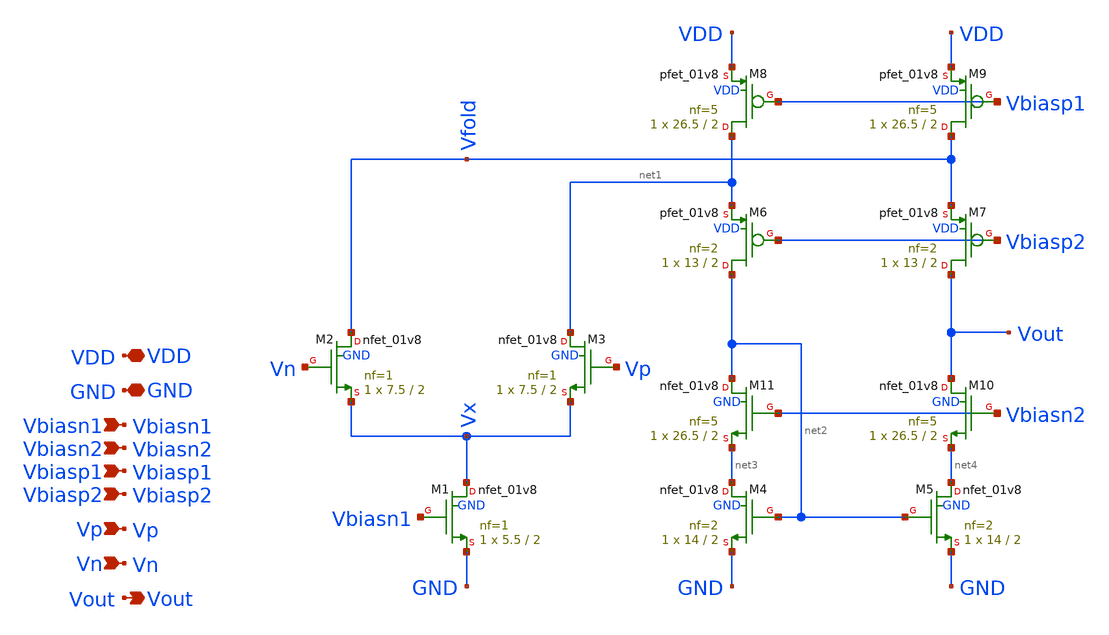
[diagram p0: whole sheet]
** sch_path: sch/cascode/ota_n.sch
**.subckt ota_n Vbiasn2 Vout VDD GND Vp Vn Vbiasp1 Vbiasp2 Vbiasn1
*.ipin Vbiasn2
*.opin Vout
*.iopin VDD
*.iopin GND
*.ipin Vp
*.ipin Vn
*.ipin Vbiasp1
*.ipin Vbiasp2
*.ipin Vbiasn1
XM3 net1 Vp Vx GND sky130_fd_pr__nfet_01v8 L=2 W=7.5 nf=1 ad='int((1 + 1)/2) * 7.5 / 1 * 0.29' as='int((1 + 2)/2) * 7.5 / 1 * 0.29'
+ pd='2*int((1 + 1)/2) * (7.5 / 1 + 0.29)' ps='2*int((1 + 2)/2) * (7.5 / 1 + 0.29)' nrd='0.29 / 7.5 ' nrs='0.29 / 7.5 '
+ sa=0 sb=0 sd=0 mult=1 m=1
XM2 Vfold Vn Vx GND sky130_fd_pr__nfet_01v8 L=2 W=7.5 nf=1 ad='int((1 + 1)/2) * 7.5 / 1 * 0.29' as='int((1 + 2)/2) * 7.5 / 1 * 0.29'
+ pd='2*int((1 + 1)/2) * (7.5 / 1 + 0.29)' ps='2*int((1 + 2)/2) * (7.5 / 1 + 0.29)' nrd='0.29 / 7.5 ' nrs='0.29 / 7.5 '
+ sa=0 sb=0 sd=0 mult=1 m=1
XM4 net3 net2 GND GND sky130_fd_pr__nfet_01v8 L=2 W=14 nf=2 ad='int((2 + 1)/2) * 14 / 2 * 0.29' as='int((2 + 2)/2) * 14 / 2 * 0.29'
+ pd='2*int((2 + 1)/2) * (14 / 2 + 0.29)' ps='2*int((2 + 2)/2) * (14 / 2 + 0.29)' nrd='0.29 / 14 ' nrs='0.29 / 14 '
+ sa=0 sb=0 sd=0 mult=1 m=1
XM5 net4 net2 GND GND sky130_fd_pr__nfet_01v8 L=2 W=14 nf=2 ad='int((2 + 1)/2) * 14 / 2 * 0.29' as='int((2 + 2)/2) * 14 / 2 * 0.29'
+ pd='2*int((2 + 1)/2) * (14 / 2 + 0.29)' ps='2*int((2 + 2)/2) * (14 / 2 + 0.29)' nrd='0.29 / 14 ' nrs='0.29 / 14 '
+ sa=0 sb=0 sd=0 mult=1 m=1
XM8 net1 Vbiasp1 VDD VDD sky130_fd_pr__pfet_01v8 L=2 W=26.5 nf=5 ad='int((5 + 1)/2) * 26.5 / 5 * 0.29'
+ as='int((5 + 2)/2) * 26.5 / 5 * 0.29' pd='2*int((5 + 1)/2) * (26.5 / 5 + 0.29)' ps='2*int((5 + 2)/2) * (26.5 / 5 + 0.29)'
+ nrd='0.29 / 26.5 ' nrs='0.29 / 26.5 ' sa=0 sb=0 sd=0 mult=1 m=1
XM9 Vfold Vbiasp1 VDD VDD sky130_fd_pr__pfet_01v8 L=2 W=26.5 nf=5 ad='int((5 + 1)/2) * 26.5 / 5 * 0.29'
+ as='int((5 + 2)/2) * 26.5 / 5 * 0.29' pd='2*int((5 + 1)/2) * (26.5 / 5 + 0.29)' ps='2*int((5 + 2)/2) * (26.5 / 5 + 0.29)'
+ nrd='0.29 / 26.5 ' nrs='0.29 / 26.5 ' sa=0 sb=0 sd=0 mult=1 m=1
XM1 Vx Vbiasn1 GND GND sky130_fd_pr__nfet_01v8 L=2 W=5.5 nf=1 ad='int((1 + 1)/2) * 5.5 / 1 * 0.29' as='int((1 + 2)/2) * 5.5 / 1 * 0.29'
+ pd='2*int((1 + 1)/2) * (5.5 / 1 + 0.29)' ps='2*int((1 + 2)/2) * (5.5 / 1 + 0.29)' nrd='0.29 / 5.5 ' nrs='0.29 / 5.5 '
+ sa=0 sb=0 sd=0 mult=1 m=1
XM6 net2 Vbiasp2 net1 VDD sky130_fd_pr__pfet_01v8 L=2 W=13 nf=2 ad='int((2 + 1)/2) * 13 / 2 * 0.29' as='int((2 + 2)/2) * 13 / 2 * 0.29'
+ pd='2*int((2 + 1)/2) * (13 / 2 + 0.29)' ps='2*int((2 + 2)/2) * (13 / 2 + 0.29)' nrd='0.29 / 13 ' nrs='0.29 / 13 '
+ sa=0 sb=0 sd=0 mult=1 m=1
XM7 Vout Vbiasp2 Vfold VDD sky130_fd_pr__pfet_01v8 L=2 W=13 nf=2 ad='int((2 + 1)/2) * 13 / 2 * 0.29'
+ as='int((2 + 2)/2) * 13 / 2 * 0.29' pd='2*int((2 + 1)/2) * (13 / 2 + 0.29)' ps='2*int((2 + 2)/2) * (13 / 2 + 0.29)'
+ nrd='0.29 / 13 ' nrs='0.29 / 13 ' sa=0 sb=0 sd=0 mult=1 m=1
XM10 Vout Vbiasn2 net4 GND sky130_fd_pr__nfet_01v8 L=2 W=26.5 nf=5 ad='int((5 + 1)/2) * 26.5 / 5 * 0.29'
+ as='int((5 + 2)/2) * 26.5 / 5 * 0.29' pd='2*int((5 + 1)/2) * (26.5 / 5 + 0.29)' ps='2*int((5 + 2)/2) * (26.5 / 5 + 0.29)'
+ nrd='0.29 / 26.5 ' nrs='0.29 / 26.5 ' sa=0 sb=0 sd=0 mult=1 m=1
XM11 net2 Vbiasn2 net3 GND sky130_fd_pr__nfet_01v8 L=2 W=26.5 nf=5 ad='int((5 + 1)/2) * 26.5 / 5 * 0.29'
+ as='int((5 + 2)/2) * 26.5 / 5 * 0.29' pd='2*int((5 + 1)/2) * (26.5 / 5 + 0.29)' ps='2*int((5 + 2)/2) * (26.5 / 5 + 0.29)'
+ nrd='0.29 / 26.5 ' nrs='0.29 / 26.5 ' sa=0 sb=0 sd=0 mult=1 m=1
**.ends
.end
